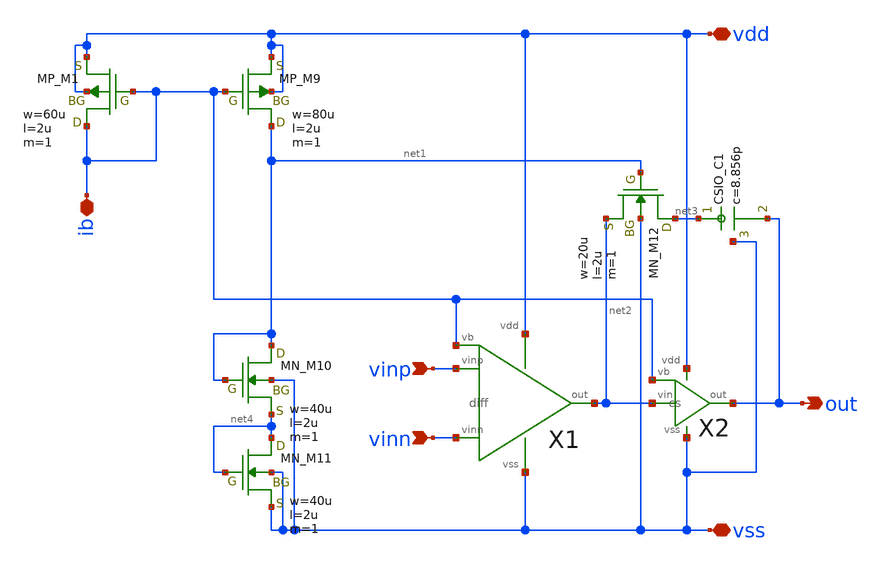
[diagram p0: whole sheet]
** sch_path: member_project/opamp/houta/opamp.sch
**.subckt opamp vinp vinn out vdd vss ib
*.ipin vinp
*.ipin vinn
*.opin out
*.iopin vdd
*.iopin vss
*.iopin ib
X1 vinp vinn net2 vdd vss ib diff
X2 net2 ib out vdd vss cs
XM9 net1 ib vdd vdd PMOS w=80u l=2u as=0 ad=0 ps=0 pd=0 nrd=0 nrs=0 m=1
XM12 net3 net1 net2 vss NMOS w=20u l=2u as=0 ad=0 ps=0 pd=0 nrd=0 nrs=0 m=1
XM1 ib ib vdd vdd PMOS w=60u l=2u as=0 ad=0 ps=0 pd=0 nrd=0 nrs=0 m=1
XM10 net1 net1 net4 vss NMOS w=40u l=2u as=0 ad=0 ps=0 pd=0 nrd=0 nrs=0 m=1
XM11 net4 net4 vss vss NMOS w=40u l=2u as=0 ad=0 ps=0 pd=0 nrd=0 nrs=0 m=1
XC1 net3 out vss F_CSIO c=8.856p x=120u y=120u m=1
**.ends

* expanding   symbol:  diff.sym # of pins=6
** sym_path: diff.sym
** sch_path: diff.sch
.subckt diff vinp vinn out vdd vss vb
*.ipin vinn
*.ipin vinp
*.ipin vb
*.opin out
*.iopin vdd
*.iopin vss
XM5 net2 vb vdd vdd PMOS w=220u l=2u as=0 ad=0 ps=0 pd=0 nrd=0 nrs=0 m=1
XM1 net1 vinn net2 net2 PMOS w=500u l=2u as=0 ad=0 ps=0 pd=0 nrd=0 nrs=0 m=1
XM2 out vinp net2 net2 PMOS w=500u l=2u as=0 ad=0 ps=0 pd=0 nrd=0 nrs=0 m=1
XM3 net1 net1 vss vss NMOS w=40u l=2u as=0 ad=0 ps=0 pd=0 nrd=0 nrs=0 m=1
XM4 out net1 vss vss NMOS w=40u l=2u as=0 ad=0 ps=0 pd=0 nrd=0 nrs=0 m=1
.ends


* expanding   symbol:  cs.sym # of pins=5
** sym_path: cs.sym
** sch_path: cs.sch
.subckt cs vin vb out vdd vss
*.ipin vb
*.ipin vin
*.opin out
*.iopin vss
*.iopin vdd
XM6 out vb vdd vdd PMOS w=280u l=2u as=0 ad=0 ps=0 pd=0 nrd=0 nrs=0 m=1
XM7 out vin vss vss NMOS w=100u l=2u as=0 ad=0 ps=0 pd=0 nrd=0 nrs=0 m=1
.ends

.end
